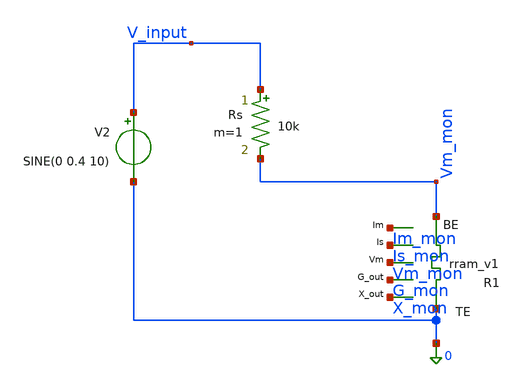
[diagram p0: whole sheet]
** sch_path: tb_monitor_comparison.sch
**.subckt tb_monitor_comparison
V2 V_input 0 SINE(0 0.4 10)
XR1 0 Vm_mon X_mon G_mon Vm_mon Is_mon Im_mon rram_v1
Rs V_input Vm_mon 10k m=1
**** begin user architecture code


*================================================================
* Simulation setup - matches Python parameters
*================================================================
.options num_threads=8
.options method=gear
.options maxstep=20u
.options reltol=1e-4
.options abstol=1e-12

* Transient analysis
.tran 20u 75m

.control
	save all
	run
	write tb_monitor_comparison.raw

.endc



*================================================================
* RRAM Model with Internal Variable Monitoring
*================================================================

.control
pre_osdi /foss/designs/Capibara_tuto/MEMS/rram_v1_with_monitors.osdi
.endc

*----------------------------------------------------------------
* Subcircuit with monitoring outputs
*----------------------------------------------------------------
.subckt rram_v1 TE BE X_OUT G_OUT VM_OUT IS_OUT IM_OUT
N1 TE BE X_OUT G_OUT VM_OUT IS_OUT IM_OUT rram_v1_model
.ends rram_v1

*----------------------------------------------------------------
* Model parameters (match Python exactly)
*----------------------------------------------------------------
.model rram_v1_model rram_v1_va   x0=0.0

**** end user architecture code
**.ends
.end
